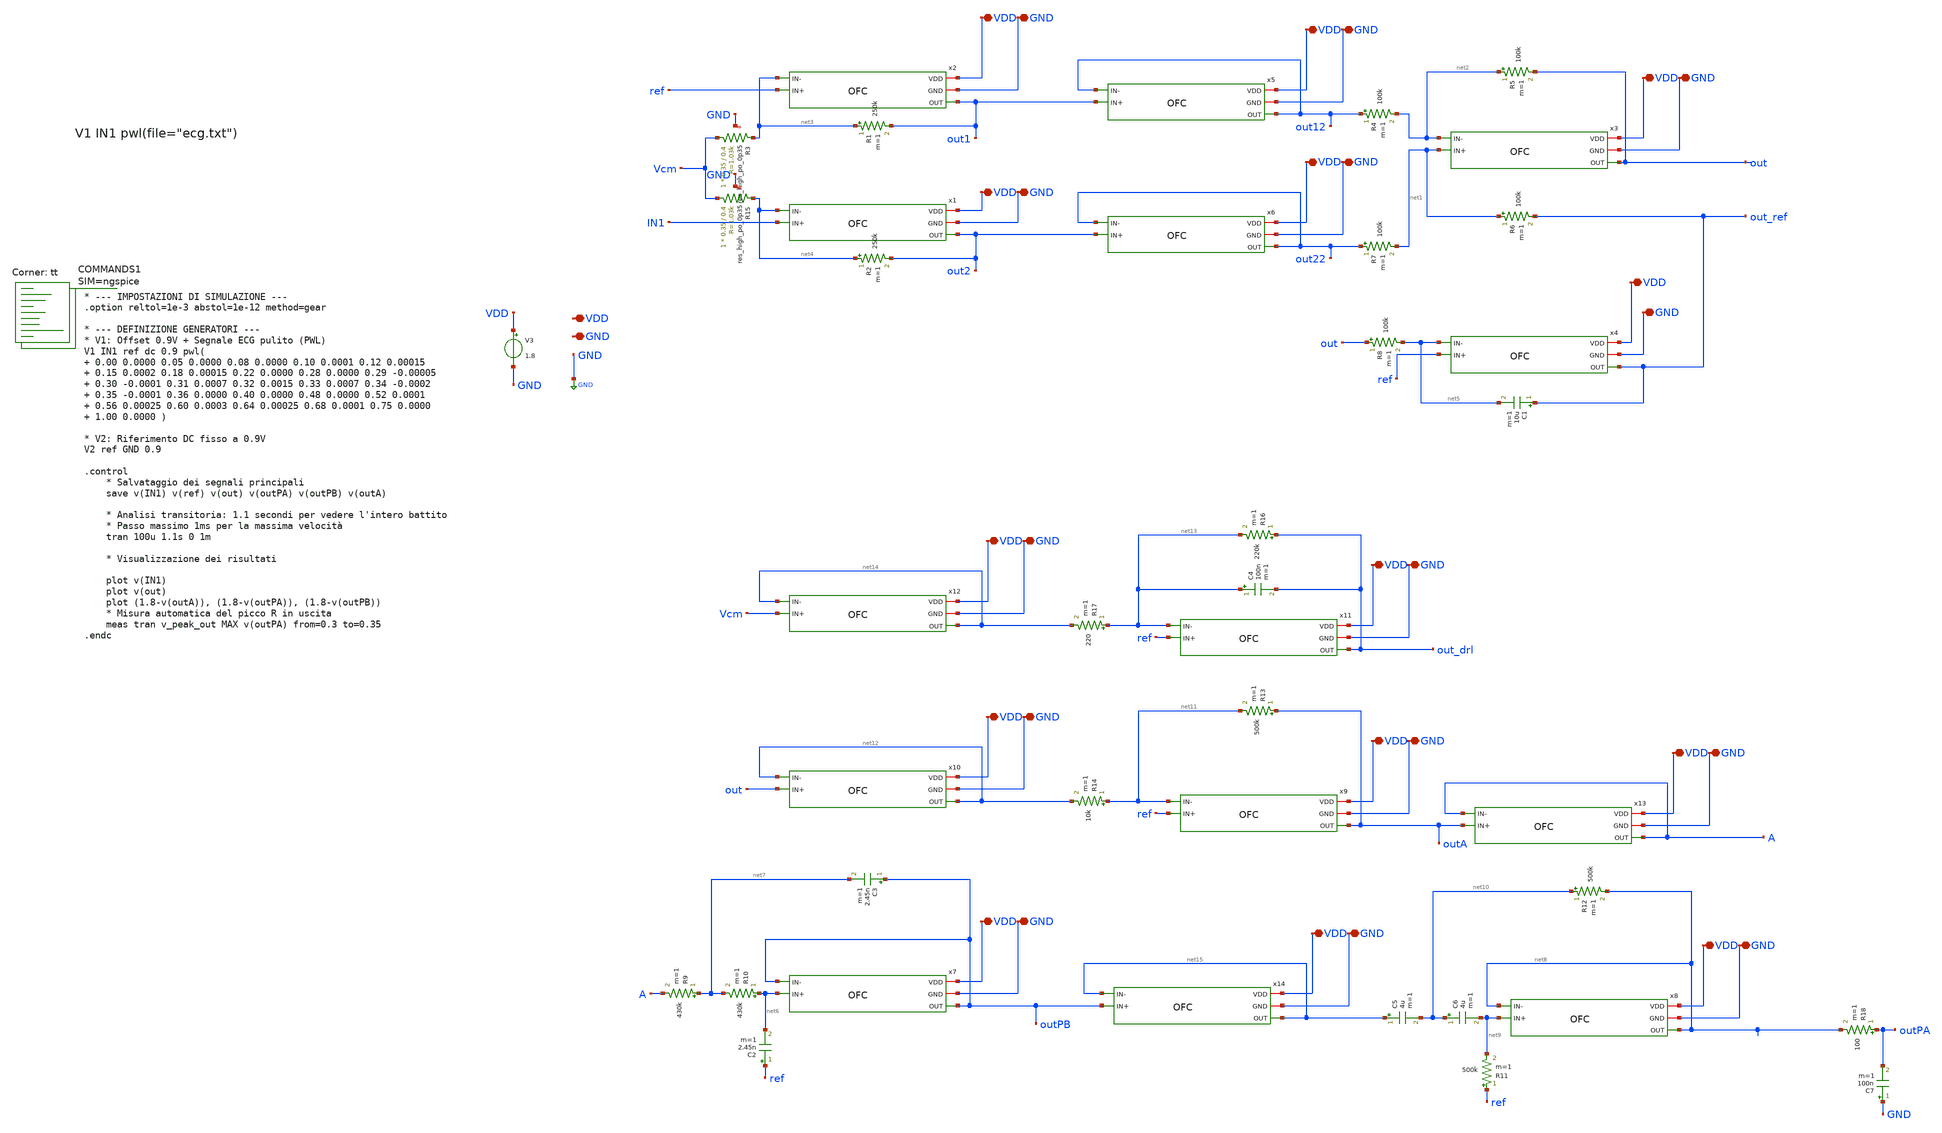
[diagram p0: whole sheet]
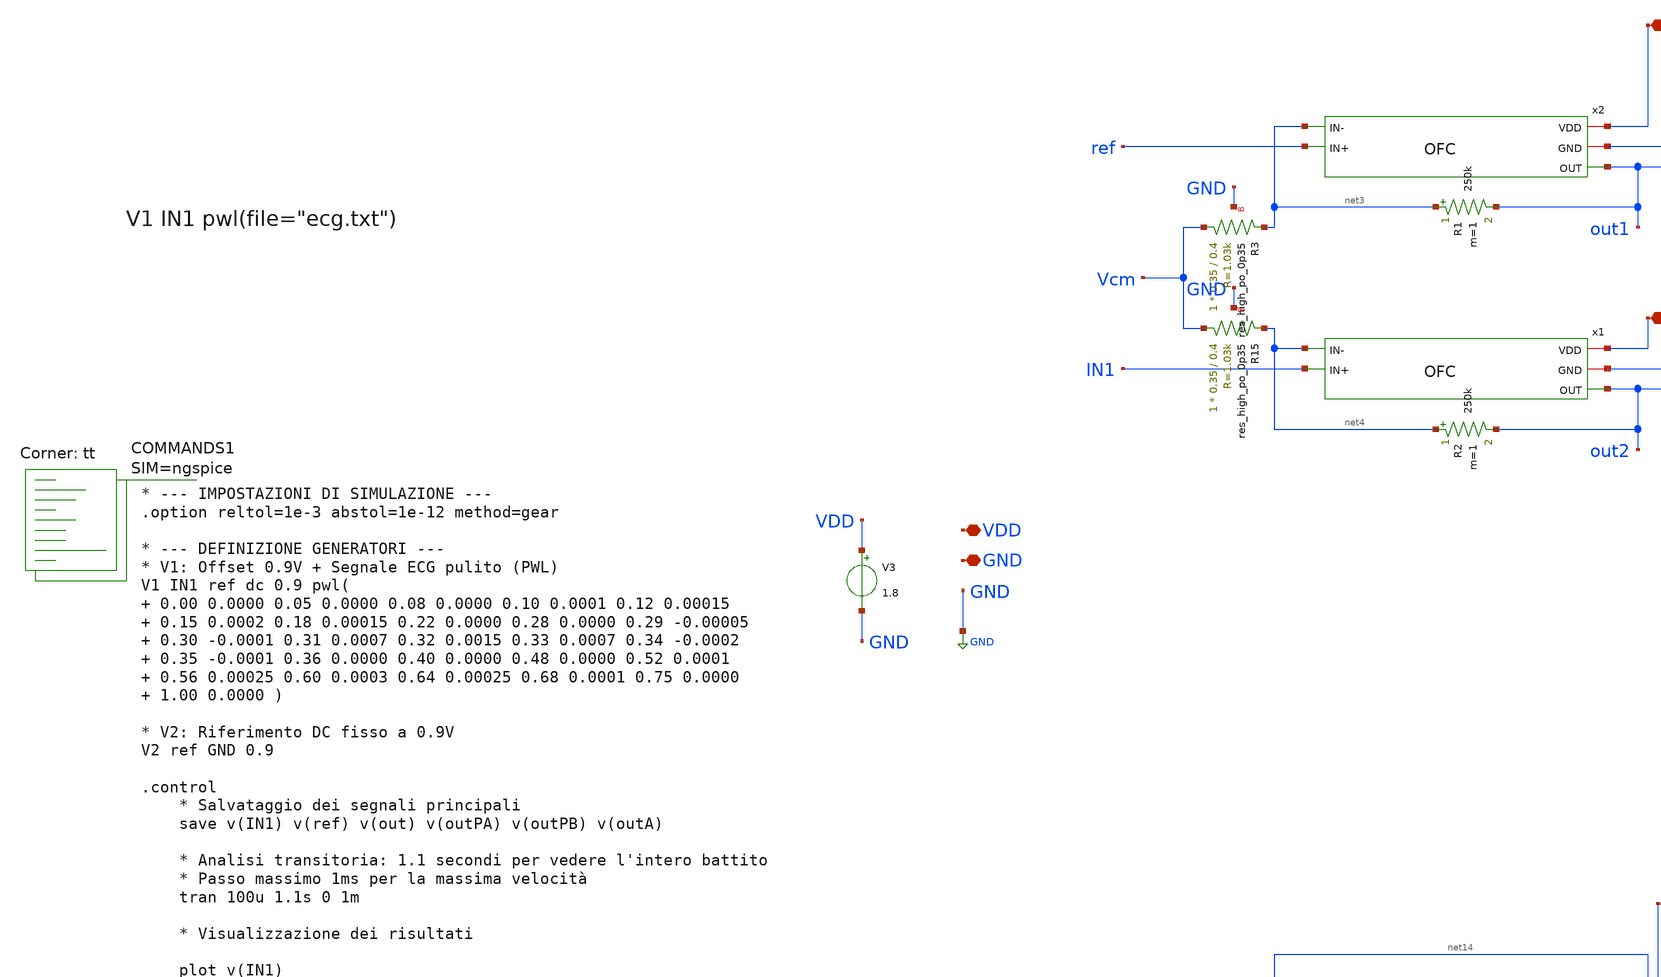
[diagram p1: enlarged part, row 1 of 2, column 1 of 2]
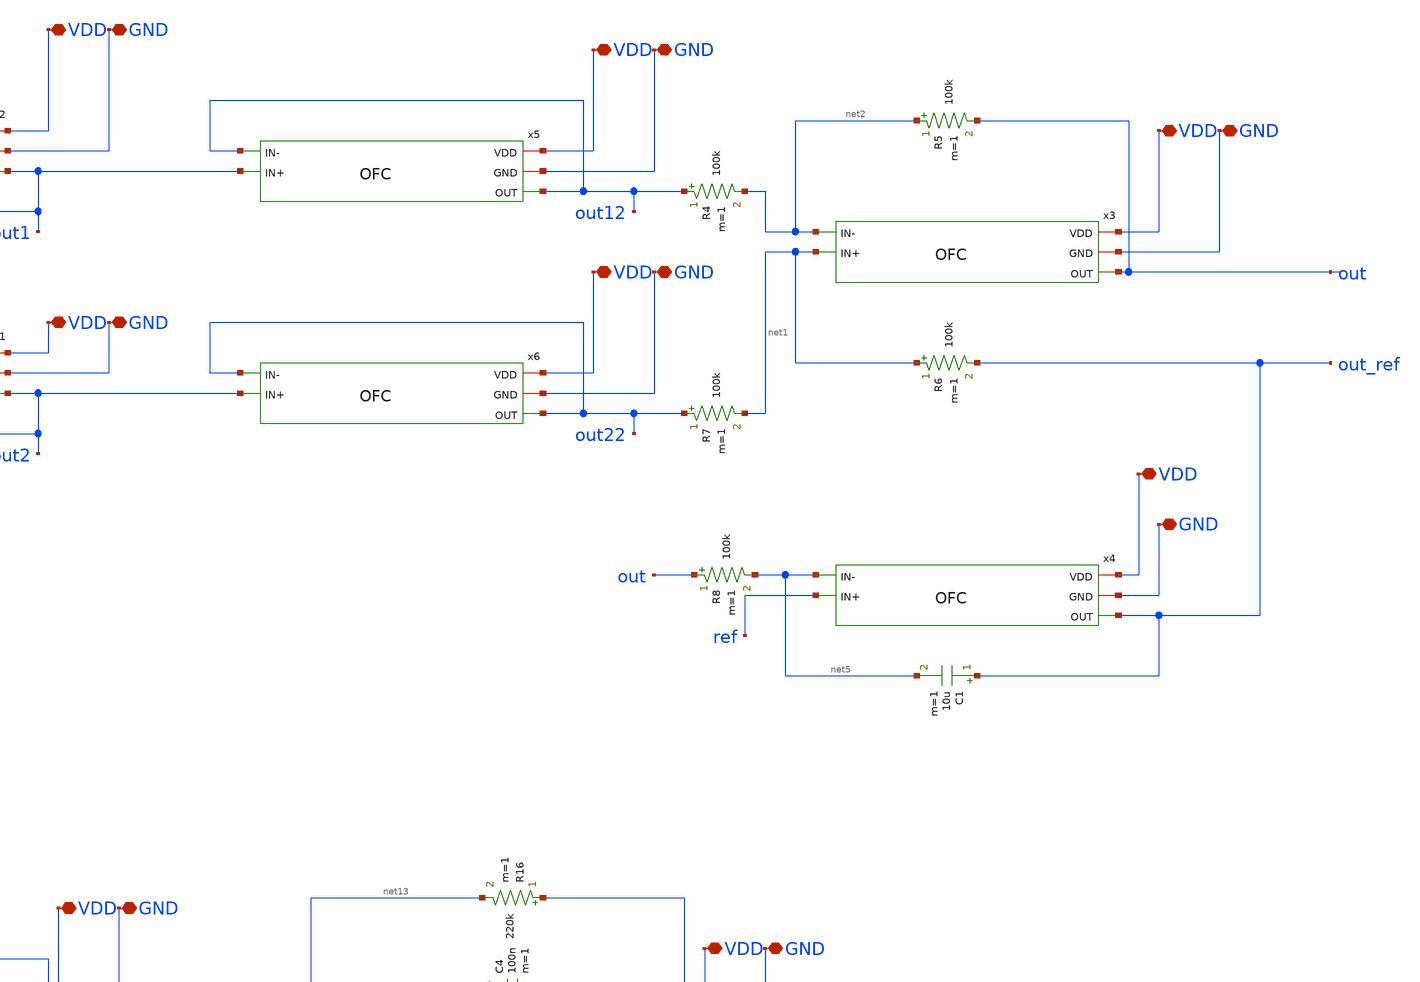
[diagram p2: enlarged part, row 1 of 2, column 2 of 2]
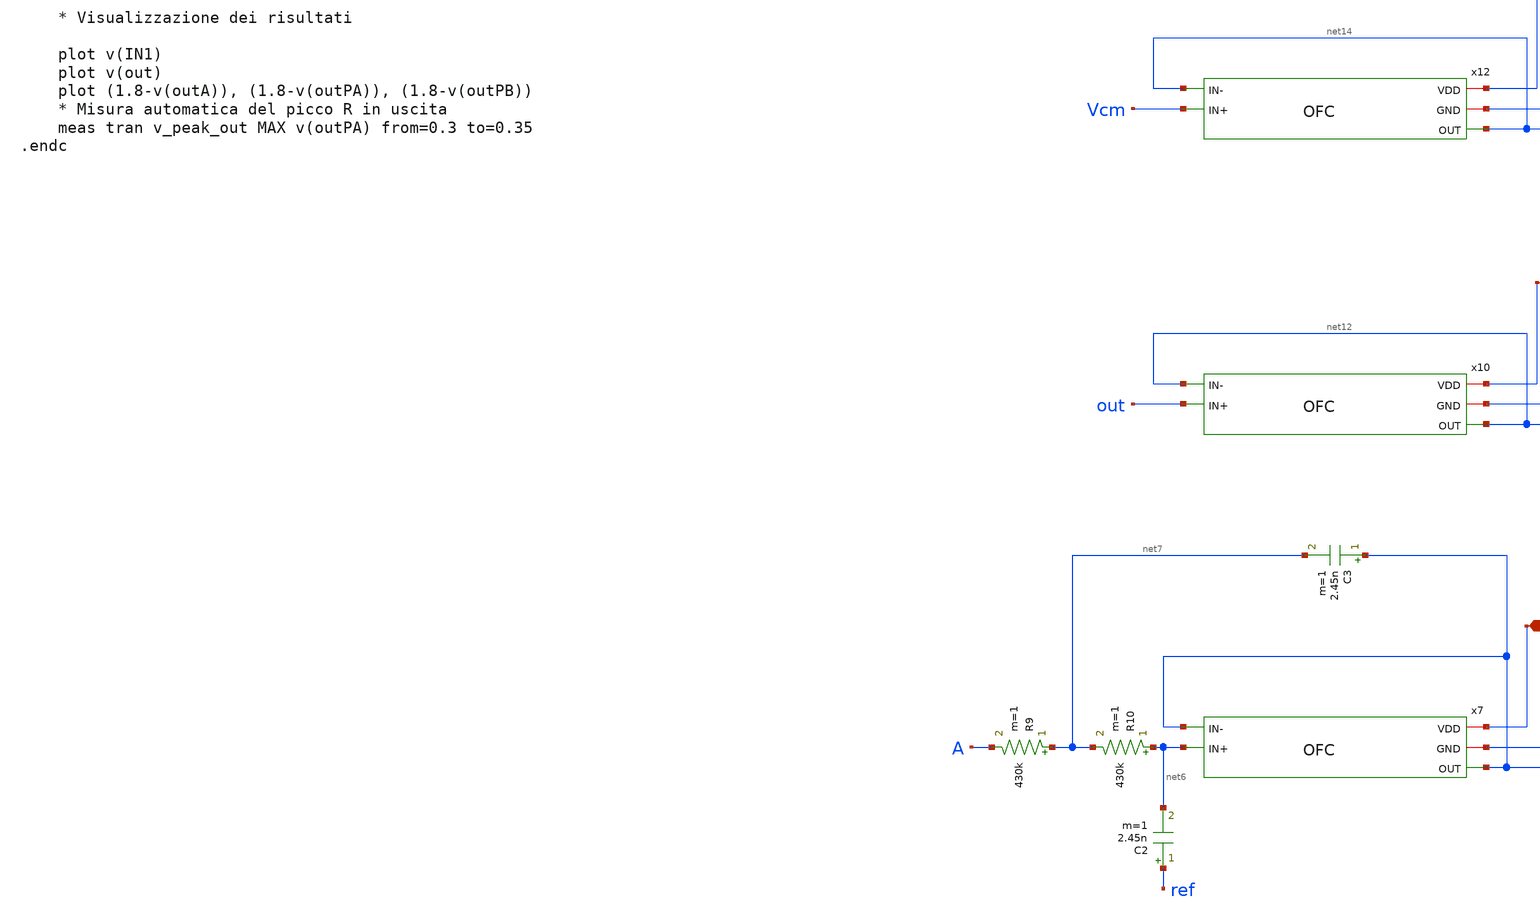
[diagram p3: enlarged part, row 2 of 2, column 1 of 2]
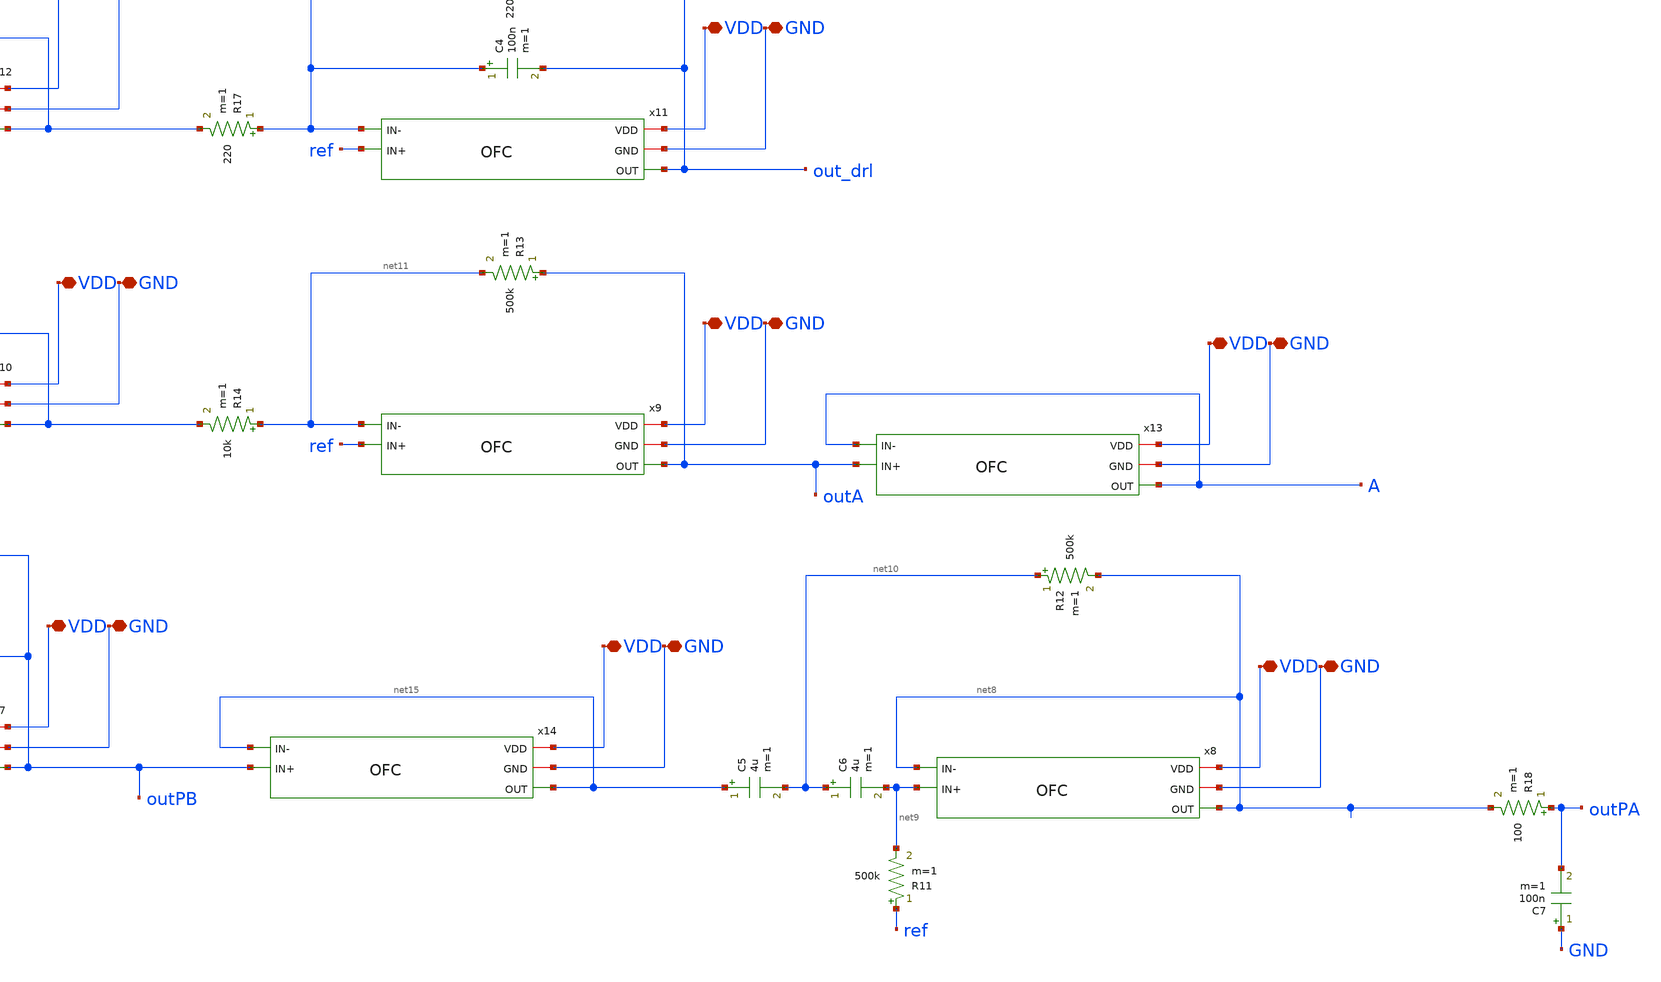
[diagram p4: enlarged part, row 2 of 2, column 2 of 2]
** sch_path: xschem/ecg_pwl.sch
**.subckt ecg_pwl VDD GND VDD VDD GND GND VDD GND VDD GND VDD GND VDD GND VDD GND VDD GND VDD GND
*+ VDD GND VDD GND VDD GND VDD GND VDD GND
*.iopin VDD
*.iopin GND
*.iopin VDD
*.iopin VDD
*.iopin GND
*.iopin GND
*.iopin VDD
*.iopin GND
*.iopin VDD
*.iopin GND
*.iopin VDD
*.iopin GND
*.iopin VDD
*.iopin GND
*.iopin VDD
*.iopin GND
*.iopin VDD
*.iopin GND
*.iopin VDD
*.iopin GND
*.iopin VDD
*.iopin GND
*.iopin VDD
*.iopin GND
*.iopin VDD
*.iopin GND
*.iopin VDD
*.iopin GND
*.iopin VDD
*.iopin GND
x1 VDD GND out2 net4 IN1 OFC
x2 VDD GND out1 net3 ref OFC
x3 VDD GND out net2 net1 OFC
V3 VDD GND 1.8
R1 net3 out1 250k m=1
R2 net4 out2 250k m=1
x4 VDD GND out_ref net5 ref OFC
R6 net1 out_ref 100k m=1
R8 out net5 100k m=1
C1 out_ref net5 10u m=1
R5 net2 out 100k m=1
x5 VDD GND out12 out12 out1 OFC
x6 VDD GND out22 out22 out2 OFC
R4 out12 net2 100k m=1
R7 out22 net1 100k m=1
x7 VDD GND outPB outPB net6 OFC
R9 net7 A 430k m=1
C2 ref net6 2.45n m=1
R10 net6 net7 430k m=1
C3 outPB net7 2.45n m=1
x8 VDD GND net8 net8 net9 OFC
R11 ref net9 500k m=1
C5 net15 net10 4u m=1
C6 net10 net9 4u m=1
x9 VDD GND outA net11 ref OFC
R13 outA net11 500k m=1
R14 net11 net12 10k m=1
x10 VDD GND net12 net12 out OFC
x11 VDD GND out_drl net13 ref OFC
R16 out_drl net13 220k m=1
R17 net13 net14 220 m=1
x12 VDD GND net14 net14 Vcm OFC
C4 net13 out_drl 100n m=1
x13 VDD GND A A outA OFC
x14 VDD GND net15 net15 outPB OFC
C7 GND outPA 100n m=1
R18 outPA net8 100 m=1
R12 net10 net8 500k m=1
XR3 Vcm net3 GND sky130_fd_pr__res_high_po_0p35 L=0.4 mult=1 m=1
XR15 Vcm net4 GND sky130_fd_pr__res_high_po_0p35 L=0.4 mult=1 m=1
**** begin user architecture code


* --- IMPOSTAZIONI DI SIMULAZIONE ---
.option reltol=1e-3 abstol=1e-12 method=gear

* --- DEFINIZIONE GENERATORI ---
* V1: Offset 0.9V + Segnale ECG pulito (PWL)
V1 IN1 ref dc 0.9 pwl(   0.00 0.0000 0.05 0.0000 0.08 0.0000 0.10 0.0001 0.12 0.00015   0.15 0.0002
+ 0.18 0.00015 0.22 0.0000 0.28 0.0000 0.29 -0.00005   0.30 -0.0001 0.31 0.0007 0.32 0.0015 0.33 0.0007
+ 0.34 -0.0002   0.35 -0.0001 0.36 0.0000 0.40 0.0000 0.48 0.0000 0.52 0.0001   0.56 0.00025 0.60 0.0003
+ 0.64 0.00025 0.68 0.0001 0.75 0.0000   1.00 0.0000 )

* V2: Riferimento DC fisso a 0.9V
V2 ref GND 0.9

.control
    * Salvataggio dei segnali principali
    save v(IN1) v(ref) v(out) v(outPA) v(outPB) v(outA)

    * Analisi transitoria: 1.1 secondi per vedere l'intero battito
    * Passo massimo 1ms per la massima velocità
    tran 100u 1.1s 0 1m

    * Visualizzazione dei risultati

    plot v(IN1)
    plot v(out)
    plot (1.8-v(outA)), (1.8-v(outPA)), (1.8-v(outPB))
    * Misura automatica del picco R in uscita
    meas tran v_peak_out MAX v(outPA) from=0.3 to=0.35
.endc



.lib $::SKYWATER_MODELS/sky130.lib.spice tt
**** end user architecture code
**.ends

* expanding   symbol:  OFC.sym # of pins=5
** sym_path: OFC.sym
** sch_path: OFC.sch
.subckt OFC VDD GND OUT IN- IN+
*.iopin VDD
*.iopin GND
*.ipin IN+
*.ipin IN-
*.opin OUT
XM11 S Vb VDD VDD sky130_fd_pr__pfet_01v8_lvt L=1 W=60 nf=2 ad='int((nf+1)/2) * W/nf * 0.29' as='int((nf+2)/2)
+ * W/nf * 0.29' pd='2*int((nf+1)/2) * (W/nf + 0.29)' ps='2*int((nf+2)/2) * (W/nf + 0.29)' nrd='0.29 /
+ W' nrs='0.29 / W' sa=0 sb=0 sd=0 mult=2 m=2
XM1 D1 IN+ S S sky130_fd_pr__pfet_01v8_lvt L=10 W=25 nf=2 ad='int((nf+1)/2) * W/nf * 0.29' as='int((nf+2)/2)
+ * W/nf * 0.29' pd='2*int((nf+1)/2) * (W/nf + 0.29)' ps='2*int((nf+2)/2) * (W/nf + 0.29)' nrd='0.29 /
+ W' nrs='0.29 / W' sa=0 sb=0 sd=0 mult=2 m=2
XM2 D2 IN- S S sky130_fd_pr__pfet_01v8_lvt L=10 W=25 nf=2 ad='int((nf+1)/2) * W/nf * 0.29' as='int((nf+2)/2)
+ * W/nf * 0.29' pd='2*int((nf+1)/2) * (W/nf + 0.29)' ps='2*int((nf+2)/2) * (W/nf + 0.29)' nrd='0.29 /
+ W' nrs='0.29 / W' sa=0 sb=0 sd=0 mult=2 m=2
XM3 OUT Vc1 D2 GND sky130_fd_pr__nfet_01v8_lvt L=1 W=4 nf=1 ad='int((nf+1)/2) * W/nf * 0.29' as='int((nf+2)/2)
+ * W/nf * 0.29' pd='2*int((nf+1)/2) * (W/nf + 0.29)' ps='2*int((nf+2)/2) * (W/nf + 0.29)' nrd='0.29 /
+ W' nrs='0.29 / W' sa=0 sb=0 sd=0 mult=1 m=1
XM4 D2 Vc GND GND sky130_fd_pr__nfet_01v8_lvt L=1 W=2.8 nf=1 ad='int((nf+1)/2) * W/nf * 0.29' as='int((nf+2)/2)
+ * W/nf * 0.29' pd='2*int((nf+1)/2) * (W/nf + 0.29)' ps='2*int((nf+2)/2) * (W/nf + 0.29)' nrd='0.29 /
+ W' nrs='0.29 / W' sa=0 sb=0 sd=0 mult=1 m=1
XM5 D1 Vc GND GND sky130_fd_pr__nfet_01v8_lvt L=1 W=2.8 nf=1 ad='int((nf+1)/2) * W/nf * 0.29' as='int((nf+2)/2)
+ * W/nf * 0.29' pd='2*int((nf+1)/2) * (W/nf + 0.29)' ps='2*int((nf+2)/2) * (W/nf + 0.29)' nrd='0.29 /
+ W' nrs='0.29 / W' sa=0 sb=0 sd=0 mult=1 m=1
XM6 G Vc1 D1 GND sky130_fd_pr__nfet_01v8_lvt L=1 W=4 nf=1 ad='int((nf+1)/2) * W/nf * 0.29' as='int((nf+2)/2)
+ * W/nf * 0.29' pd='2*int((nf+1)/2) * (W/nf + 0.29)' ps='2*int((nf+2)/2) * (W/nf + 0.29)' nrd='0.29 /
+ W' nrs='0.29 / W' sa=0 sb=0 sd=0 mult=1 m=1
XM7 G Vc2 D9 D9 sky130_fd_pr__pfet_01v8_lvt L=2.23 W=3 nf=1 ad='int((nf+1)/2) * W/nf * 0.29' as='int((nf+2)/2)
+ * W/nf * 0.29' pd='2*int((nf+1)/2) * (W/nf + 0.29)' ps='2*int((nf+2)/2) * (W/nf + 0.29)' nrd='0.29 /
+ W' nrs='0.29 / W' sa=0 sb=0 sd=0 mult=1 m=1
XM9 D9 G VDD VDD sky130_fd_pr__pfet_01v8_lvt L=2.23 W=4 nf=1 ad='int((nf+1)/2) * W/nf * 0.29' as='int((nf+2)/2)
+ * W/nf * 0.29' pd='2*int((nf+1)/2) * (W/nf + 0.29)' ps='2*int((nf+2)/2) * (W/nf + 0.29)' nrd='0.29 /
+ W' nrs='0.29 / W' sa=0 sb=0 sd=0 mult=1 m=1
XM8 D10 G VDD VDD sky130_fd_pr__pfet_01v8_lvt L=2.23 W=4 nf=1 ad='int((nf+1)/2) * W/nf * 0.29' as='int((nf+2)/2)
+ * W/nf * 0.29' pd='2*int((nf+1)/2) * (W/nf + 0.29)' ps='2*int((nf+2)/2) * (W/nf + 0.29)' nrd='0.29 /
+ W' nrs='0.29 / W' sa=0 sb=0 sd=0 mult=1 m=1
XM10 OUT Vc2 D10 D10 sky130_fd_pr__pfet_01v8_lvt L=2.23 W=3 nf=1 ad='int((nf+1)/2) * W/nf * 0.29' as='int((nf+2)/2)
+ * W/nf * 0.29' pd='2*int((nf+1)/2) * (W/nf + 0.29)' ps='2*int((nf+2)/2) * (W/nf + 0.29)' nrd='0.29 /
+ W' nrs='0.29 / W' sa=0 sb=0 sd=0 mult=1 m=1
XR2 Vb VDD GND sky130_fd_pr__res_xhigh_po_0p35 L=5 mult=1 m=1
XR3 GND Vb GND sky130_fd_pr__res_xhigh_po_0p35 L=13.2 mult=1 m=1
XR1 Vc VDD GND sky130_fd_pr__res_xhigh_po_0p35 L=5 mult=1 m=1
XR4 GND Vc GND sky130_fd_pr__res_xhigh_po_0p35 L=3.07 mult=1 m=1
XR5 Vc1 VDD GND sky130_fd_pr__res_xhigh_po_0p35 L=5 mult=1 m=1
XR6 GND Vc1 GND sky130_fd_pr__res_xhigh_po_0p35 L=13.2 mult=1 m=1
XR7 Vc2 VDD GND sky130_fd_pr__res_xhigh_po_0p35 L=5 mult=1 m=1
XR8 GND Vc2 GND sky130_fd_pr__res_xhigh_po_0p35 L=1.6 mult=1 m=1
.ends

.GLOBAL GND
.end
